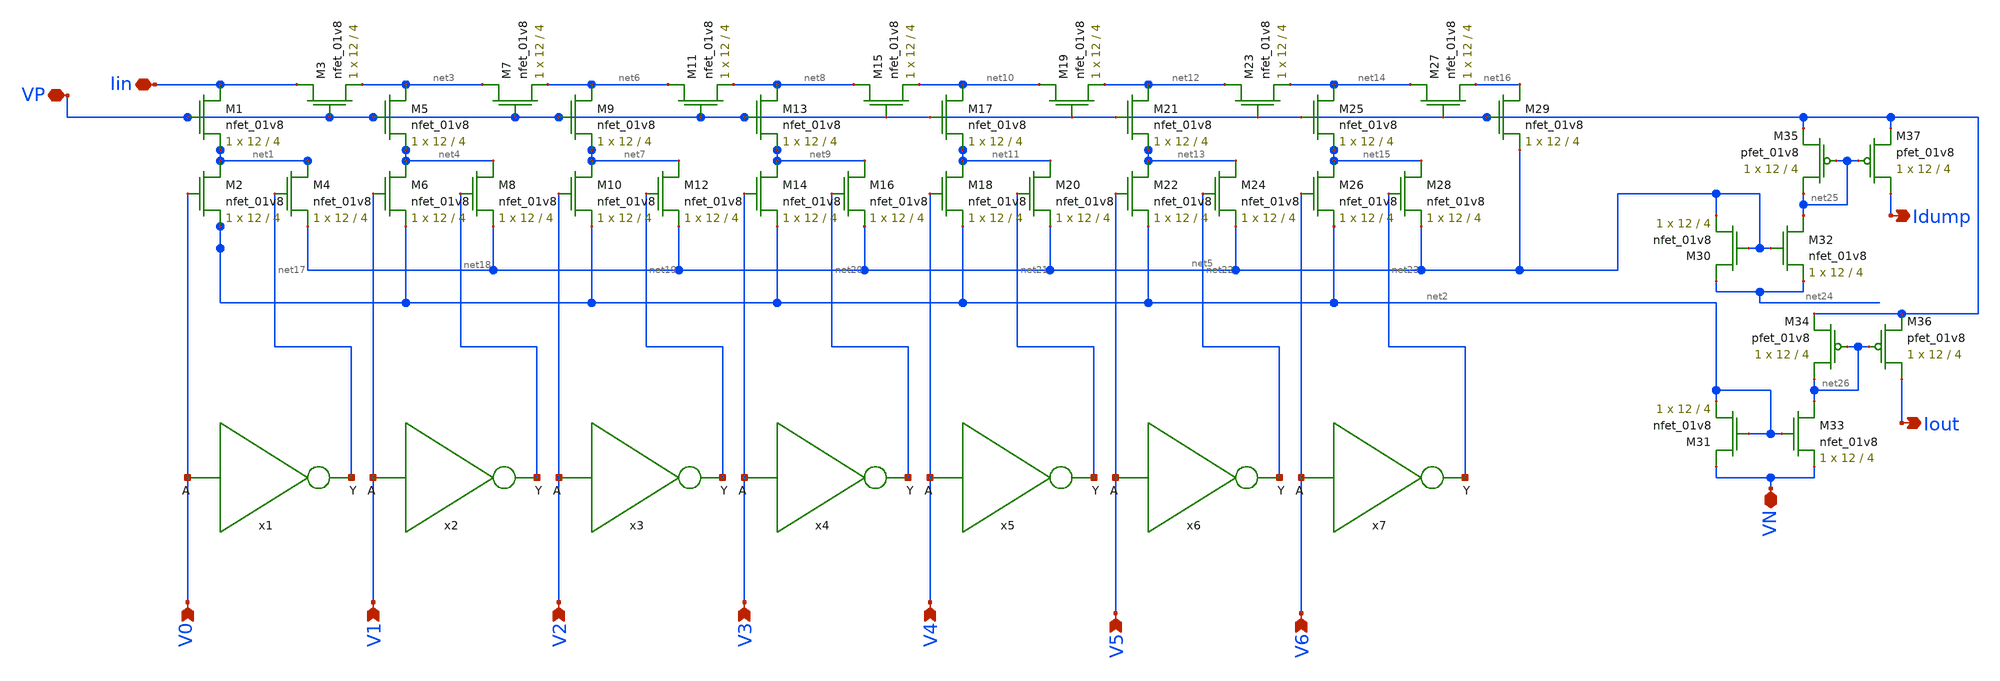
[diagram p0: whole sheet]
** sch_path: xschem/ladder.sch
**.subckt ladder V0 V1 V2 V3 V4 V5 V6 VP Iin VN Iout Idump
*.ipin V0
*.ipin V1
*.ipin V2
*.ipin V3
*.ipin V4
*.ipin V5
*.ipin V6
*.iopin VP
*.iopin Iin
*.iopin VN
*.opin Iout
*.opin Idump
XM1 Iin VP net1 GND sky130_fd_pr__nfet_01v8 L=4 W=12 nf=1 ad='int((nf+1)/2) * W/nf * 0.29' as='int((nf+2)/2) * W/nf * 0.29'
+ pd='2*int((nf+1)/2) * (W/nf + 0.29)' ps='2*int((nf+2)/2) * (W/nf + 0.29)' nrd='0.29 / W' nrs='0.29 / W'
+ sa=0 sb=0 sd=0 mult=1 m=1
XM3 Iin VP net3 GND sky130_fd_pr__nfet_01v8 L=4 W=12 nf=1 ad='int((nf+1)/2) * W/nf * 0.29' as='int((nf+2)/2) * W/nf * 0.29'
+ pd='2*int((nf+1)/2) * (W/nf + 0.29)' ps='2*int((nf+2)/2) * (W/nf + 0.29)' nrd='0.29 / W' nrs='0.29 / W'
+ sa=0 sb=0 sd=0 mult=1 m=1
XM5 net3 VP net4 GND sky130_fd_pr__nfet_01v8 L=4 W=12 nf=1 ad='int((nf+1)/2) * W/nf * 0.29' as='int((nf+2)/2) * W/nf * 0.29'
+ pd='2*int((nf+1)/2) * (W/nf + 0.29)' ps='2*int((nf+2)/2) * (W/nf + 0.29)' nrd='0.29 / W' nrs='0.29 / W'
+ sa=0 sb=0 sd=0 mult=1 m=1
XM7 net3 VP net6 GND sky130_fd_pr__nfet_01v8 L=4 W=12 nf=1 ad='int((nf+1)/2) * W/nf * 0.29' as='int((nf+2)/2) * W/nf * 0.29'
+ pd='2*int((nf+1)/2) * (W/nf + 0.29)' ps='2*int((nf+2)/2) * (W/nf + 0.29)' nrd='0.29 / W' nrs='0.29 / W'
+ sa=0 sb=0 sd=0 mult=1 m=1
XM6 net4 V1 net2 GND sky130_fd_pr__nfet_01v8 L=4 W=12 nf=1 ad='int((nf+1)/2) * W/nf * 0.29' as='int((nf+2)/2) * W/nf * 0.29'
+ pd='2*int((nf+1)/2) * (W/nf + 0.29)' ps='2*int((nf+2)/2) * (W/nf + 0.29)' nrd='0.29 / W' nrs='0.29 / W'
+ sa=0 sb=0 sd=0 mult=1 m=1
XM8 net4 net18 net5 GND sky130_fd_pr__nfet_01v8 L=4 W=12 nf=1 ad='int((nf+1)/2) * W/nf * 0.29' as='int((nf+2)/2) * W/nf * 0.29'
+ pd='2*int((nf+1)/2) * (W/nf + 0.29)' ps='2*int((nf+2)/2) * (W/nf + 0.29)' nrd='0.29 / W' nrs='0.29 / W'
+ sa=0 sb=0 sd=0 mult=1 m=1
XM2 net1 V0 net2 GND sky130_fd_pr__nfet_01v8 L=4 W=12 nf=1 ad='int((nf+1)/2) * W/nf * 0.29' as='int((nf+2)/2) * W/nf * 0.29'
+ pd='2*int((nf+1)/2) * (W/nf + 0.29)' ps='2*int((nf+2)/2) * (W/nf + 0.29)' nrd='0.29 / W' nrs='0.29 / W'
+ sa=0 sb=0 sd=0 mult=1 m=1
XM4 net1 net17 net5 GND sky130_fd_pr__nfet_01v8 L=4 W=12 nf=1 ad='int((nf+1)/2) * W/nf * 0.29' as='int((nf+2)/2) * W/nf * 0.29'
+ pd='2*int((nf+1)/2) * (W/nf + 0.29)' ps='2*int((nf+2)/2) * (W/nf + 0.29)' nrd='0.29 / W' nrs='0.29 / W'
+ sa=0 sb=0 sd=0 mult=1 m=1
XM9 net6 VP net7 GND sky130_fd_pr__nfet_01v8 L=4 W=12 nf=1 ad='int((nf+1)/2) * W/nf * 0.29' as='int((nf+2)/2) * W/nf * 0.29'
+ pd='2*int((nf+1)/2) * (W/nf + 0.29)' ps='2*int((nf+2)/2) * (W/nf + 0.29)' nrd='0.29 / W' nrs='0.29 / W'
+ sa=0 sb=0 sd=0 mult=1 m=1
XM11 net6 VP net8 GND sky130_fd_pr__nfet_01v8 L=4 W=12 nf=1 ad='int((nf+1)/2) * W/nf * 0.29' as='int((nf+2)/2) * W/nf * 0.29'
+ pd='2*int((nf+1)/2) * (W/nf + 0.29)' ps='2*int((nf+2)/2) * (W/nf + 0.29)' nrd='0.29 / W' nrs='0.29 / W'
+ sa=0 sb=0 sd=0 mult=1 m=1
XM10 net7 V2 net2 GND sky130_fd_pr__nfet_01v8 L=4 W=12 nf=1 ad='int((nf+1)/2) * W/nf * 0.29' as='int((nf+2)/2) * W/nf * 0.29'
+ pd='2*int((nf+1)/2) * (W/nf + 0.29)' ps='2*int((nf+2)/2) * (W/nf + 0.29)' nrd='0.29 / W' nrs='0.29 / W'
+ sa=0 sb=0 sd=0 mult=1 m=1
XM12 net7 net19 net5 GND sky130_fd_pr__nfet_01v8 L=4 W=12 nf=1 ad='int((nf+1)/2) * W/nf * 0.29' as='int((nf+2)/2) * W/nf * 0.29'
+ pd='2*int((nf+1)/2) * (W/nf + 0.29)' ps='2*int((nf+2)/2) * (W/nf + 0.29)' nrd='0.29 / W' nrs='0.29 / W'
+ sa=0 sb=0 sd=0 mult=1 m=1
XM13 net8 VP net9 GND sky130_fd_pr__nfet_01v8 L=4 W=12 nf=1 ad='int((nf+1)/2) * W/nf * 0.29' as='int((nf+2)/2) * W/nf * 0.29'
+ pd='2*int((nf+1)/2) * (W/nf + 0.29)' ps='2*int((nf+2)/2) * (W/nf + 0.29)' nrd='0.29 / W' nrs='0.29 / W'
+ sa=0 sb=0 sd=0 mult=1 m=1
XM15 net8 VP net10 GND sky130_fd_pr__nfet_01v8 L=4 W=12 nf=1 ad='int((nf+1)/2) * W/nf * 0.29' as='int((nf+2)/2) * W/nf * 0.29'
+ pd='2*int((nf+1)/2) * (W/nf + 0.29)' ps='2*int((nf+2)/2) * (W/nf + 0.29)' nrd='0.29 / W' nrs='0.29 / W'
+ sa=0 sb=0 sd=0 mult=1 m=1
XM14 net9 V3 net2 GND sky130_fd_pr__nfet_01v8 L=4 W=12 nf=1 ad='int((nf+1)/2) * W/nf * 0.29' as='int((nf+2)/2) * W/nf * 0.29'
+ pd='2*int((nf+1)/2) * (W/nf + 0.29)' ps='2*int((nf+2)/2) * (W/nf + 0.29)' nrd='0.29 / W' nrs='0.29 / W'
+ sa=0 sb=0 sd=0 mult=1 m=1
XM16 net9 net20 net5 GND sky130_fd_pr__nfet_01v8 L=4 W=12 nf=1 ad='int((nf+1)/2) * W/nf * 0.29' as='int((nf+2)/2) * W/nf * 0.29'
+ pd='2*int((nf+1)/2) * (W/nf + 0.29)' ps='2*int((nf+2)/2) * (W/nf + 0.29)' nrd='0.29 / W' nrs='0.29 / W'
+ sa=0 sb=0 sd=0 mult=1 m=1
XM17 net10 VP net11 GND sky130_fd_pr__nfet_01v8 L=4 W=12 nf=1 ad='int((nf+1)/2) * W/nf * 0.29' as='int((nf+2)/2) * W/nf * 0.29'
+ pd='2*int((nf+1)/2) * (W/nf + 0.29)' ps='2*int((nf+2)/2) * (W/nf + 0.29)' nrd='0.29 / W' nrs='0.29 / W'
+ sa=0 sb=0 sd=0 mult=1 m=1
XM19 net10 VP net12 GND sky130_fd_pr__nfet_01v8 L=4 W=12 nf=1 ad='int((nf+1)/2) * W/nf * 0.29' as='int((nf+2)/2) * W/nf * 0.29'
+ pd='2*int((nf+1)/2) * (W/nf + 0.29)' ps='2*int((nf+2)/2) * (W/nf + 0.29)' nrd='0.29 / W' nrs='0.29 / W'
+ sa=0 sb=0 sd=0 mult=1 m=1
XM18 net11 V4 net2 GND sky130_fd_pr__nfet_01v8 L=4 W=12 nf=1 ad='int((nf+1)/2) * W/nf * 0.29' as='int((nf+2)/2) * W/nf * 0.29'
+ pd='2*int((nf+1)/2) * (W/nf + 0.29)' ps='2*int((nf+2)/2) * (W/nf + 0.29)' nrd='0.29 / W' nrs='0.29 / W'
+ sa=0 sb=0 sd=0 mult=1 m=1
XM20 net11 net21 net5 GND sky130_fd_pr__nfet_01v8 L=4 W=12 nf=1 ad='int((nf+1)/2) * W/nf * 0.29' as='int((nf+2)/2) * W/nf * 0.29'
+ pd='2*int((nf+1)/2) * (W/nf + 0.29)' ps='2*int((nf+2)/2) * (W/nf + 0.29)' nrd='0.29 / W' nrs='0.29 / W'
+ sa=0 sb=0 sd=0 mult=1 m=1
XM21 net12 VP net13 GND sky130_fd_pr__nfet_01v8 L=4 W=12 nf=1 ad='int((nf+1)/2) * W/nf * 0.29' as='int((nf+2)/2) * W/nf * 0.29'
+ pd='2*int((nf+1)/2) * (W/nf + 0.29)' ps='2*int((nf+2)/2) * (W/nf + 0.29)' nrd='0.29 / W' nrs='0.29 / W'
+ sa=0 sb=0 sd=0 mult=1 m=1
XM23 net12 VP net14 GND sky130_fd_pr__nfet_01v8 L=4 W=12 nf=1 ad='int((nf+1)/2) * W/nf * 0.29' as='int((nf+2)/2) * W/nf * 0.29'
+ pd='2*int((nf+1)/2) * (W/nf + 0.29)' ps='2*int((nf+2)/2) * (W/nf + 0.29)' nrd='0.29 / W' nrs='0.29 / W'
+ sa=0 sb=0 sd=0 mult=1 m=1
XM22 net13 V5 net2 GND sky130_fd_pr__nfet_01v8 L=4 W=12 nf=1 ad='int((nf+1)/2) * W/nf * 0.29' as='int((nf+2)/2) * W/nf * 0.29'
+ pd='2*int((nf+1)/2) * (W/nf + 0.29)' ps='2*int((nf+2)/2) * (W/nf + 0.29)' nrd='0.29 / W' nrs='0.29 / W'
+ sa=0 sb=0 sd=0 mult=1 m=1
XM24 net13 net22 net5 GND sky130_fd_pr__nfet_01v8 L=4 W=12 nf=1 ad='int((nf+1)/2) * W/nf * 0.29' as='int((nf+2)/2) * W/nf * 0.29'
+ pd='2*int((nf+1)/2) * (W/nf + 0.29)' ps='2*int((nf+2)/2) * (W/nf + 0.29)' nrd='0.29 / W' nrs='0.29 / W'
+ sa=0 sb=0 sd=0 mult=1 m=1
XM25 net14 VP net15 GND sky130_fd_pr__nfet_01v8 L=4 W=12 nf=1 ad='int((nf+1)/2) * W/nf * 0.29' as='int((nf+2)/2) * W/nf * 0.29'
+ pd='2*int((nf+1)/2) * (W/nf + 0.29)' ps='2*int((nf+2)/2) * (W/nf + 0.29)' nrd='0.29 / W' nrs='0.29 / W'
+ sa=0 sb=0 sd=0 mult=1 m=1
XM27 net14 VP net16 GND sky130_fd_pr__nfet_01v8 L=4 W=12 nf=1 ad='int((nf+1)/2) * W/nf * 0.29' as='int((nf+2)/2) * W/nf * 0.29'
+ pd='2*int((nf+1)/2) * (W/nf + 0.29)' ps='2*int((nf+2)/2) * (W/nf + 0.29)' nrd='0.29 / W' nrs='0.29 / W'
+ sa=0 sb=0 sd=0 mult=1 m=1
XM26 net15 V6 net2 GND sky130_fd_pr__nfet_01v8 L=4 W=12 nf=1 ad='int((nf+1)/2) * W/nf * 0.29' as='int((nf+2)/2) * W/nf * 0.29'
+ pd='2*int((nf+1)/2) * (W/nf + 0.29)' ps='2*int((nf+2)/2) * (W/nf + 0.29)' nrd='0.29 / W' nrs='0.29 / W'
+ sa=0 sb=0 sd=0 mult=1 m=1
XM28 net15 net23 net5 GND sky130_fd_pr__nfet_01v8 L=4 W=12 nf=1 ad='int((nf+1)/2) * W/nf * 0.29' as='int((nf+2)/2) * W/nf * 0.29'
+ pd='2*int((nf+1)/2) * (W/nf + 0.29)' ps='2*int((nf+2)/2) * (W/nf + 0.29)' nrd='0.29 / W' nrs='0.29 / W'
+ sa=0 sb=0 sd=0 mult=1 m=1
XM29 net16 VP net5 GND sky130_fd_pr__nfet_01v8 L=4 W=12 nf=1 ad='int((nf+1)/2) * W/nf * 0.29' as='int((nf+2)/2) * W/nf * 0.29'
+ pd='2*int((nf+1)/2) * (W/nf + 0.29)' ps='2*int((nf+2)/2) * (W/nf + 0.29)' nrd='0.29 / W' nrs='0.29 / W'
+ sa=0 sb=0 sd=0 mult=1 m=1
x1 net17 V0 inverter
x2 net18 V1 inverter
x3 net19 V2 inverter
x4 net20 V3 inverter
x5 net21 V4 inverter
x6 net22 V5 inverter
x7 net23 V6 inverter
XM30 net24 net5 net5 GND sky130_fd_pr__nfet_01v8 L=4 W=12 nf=1 ad='int((nf+1)/2) * W/nf * 0.29' as='int((nf+2)/2) * W/nf * 0.29'
+ pd='2*int((nf+1)/2) * (W/nf + 0.29)' ps='2*int((nf+2)/2) * (W/nf + 0.29)' nrd='0.29 / W' nrs='0.29 / W'
+ sa=0 sb=0 sd=0 mult=1 m=1
XM31 VN net2 net2 GND sky130_fd_pr__nfet_01v8 L=4 W=12 nf=1 ad='int((nf+1)/2) * W/nf * 0.29' as='int((nf+2)/2) * W/nf * 0.29'
+ pd='2*int((nf+1)/2) * (W/nf + 0.29)' ps='2*int((nf+2)/2) * (W/nf + 0.29)' nrd='0.29 / W' nrs='0.29 / W'
+ sa=0 sb=0 sd=0 mult=1 m=1
XM32 net25 net5 net24 GND sky130_fd_pr__nfet_01v8 L=4 W=12 nf=1 ad='int((nf+1)/2) * W/nf * 0.29' as='int((nf+2)/2) * W/nf * 0.29'
+ pd='2*int((nf+1)/2) * (W/nf + 0.29)' ps='2*int((nf+2)/2) * (W/nf + 0.29)' nrd='0.29 / W' nrs='0.29 / W'
+ sa=0 sb=0 sd=0 mult=1 m=1
XM33 net26 net2 VN GND sky130_fd_pr__nfet_01v8 L=4 W=12 nf=1 ad='int((nf+1)/2) * W/nf * 0.29' as='int((nf+2)/2) * W/nf * 0.29'
+ pd='2*int((nf+1)/2) * (W/nf + 0.29)' ps='2*int((nf+2)/2) * (W/nf + 0.29)' nrd='0.29 / W' nrs='0.29 / W'
+ sa=0 sb=0 sd=0 mult=1 m=1
XM35 net25 net25 VP VDD sky130_fd_pr__pfet_01v8 L=4 W=12 nf=1 ad='int((nf+1)/2) * W/nf * 0.29' as='int((nf+2)/2) * W/nf * 0.29'
+ pd='2*int((nf+1)/2) * (W/nf + 0.29)' ps='2*int((nf+2)/2) * (W/nf + 0.29)' nrd='0.29 / W' nrs='0.29 / W'
+ sa=0 sb=0 sd=0 mult=1 m=1
XM37 Idump net25 VP VDD sky130_fd_pr__pfet_01v8 L=4 W=12 nf=1 ad='int((nf+1)/2) * W/nf * 0.29' as='int((nf+2)/2) * W/nf * 0.29'
+ pd='2*int((nf+1)/2) * (W/nf + 0.29)' ps='2*int((nf+2)/2) * (W/nf + 0.29)' nrd='0.29 / W' nrs='0.29 / W'
+ sa=0 sb=0 sd=0 mult=1 m=1
XM34 net26 net26 VP VDD sky130_fd_pr__pfet_01v8 L=4 W=12 nf=1 ad='int((nf+1)/2) * W/nf * 0.29' as='int((nf+2)/2) * W/nf * 0.29'
+ pd='2*int((nf+1)/2) * (W/nf + 0.29)' ps='2*int((nf+2)/2) * (W/nf + 0.29)' nrd='0.29 / W' nrs='0.29 / W'
+ sa=0 sb=0 sd=0 mult=1 m=1
XM36 Iout net26 VP VDD sky130_fd_pr__pfet_01v8 L=4 W=12 nf=1 ad='int((nf+1)/2) * W/nf * 0.29' as='int((nf+2)/2) * W/nf * 0.29'
+ pd='2*int((nf+1)/2) * (W/nf + 0.29)' ps='2*int((nf+2)/2) * (W/nf + 0.29)' nrd='0.29 / W' nrs='0.29 / W'
+ sa=0 sb=0 sd=0 mult=1 m=1
**.ends

* expanding   symbol:  ./inverter.sym # of pins=2
** sym_path: xschem/inverter.sym
** sch_path: xschem/inverter.sch
.subckt inverter Y A
*.ipin A
*.opin Y
XM1 Y A VDD VDD sky130_fd_pr__pfet_01v8 L=0.15 W=1 nf=1 ad='int((nf+1)/2) * W/nf * 0.29' as='int((nf+2)/2) * W/nf * 0.29'
+ pd='2*int((nf+1)/2) * (W/nf + 0.29)' ps='2*int((nf+2)/2) * (W/nf + 0.29)' nrd='0.29 / W' nrs='0.29 / W'
+ sa=0 sb=0 sd=0 mult=1 m=1
XM2 Y A GND GND sky130_fd_pr__nfet_01v8 L=0.15 W=1 nf=1 ad='int((nf+1)/2) * W/nf * 0.29' as='int((nf+2)/2) * W/nf * 0.29'
+ pd='2*int((nf+1)/2) * (W/nf + 0.29)' ps='2*int((nf+2)/2) * (W/nf + 0.29)' nrd='0.29 / W' nrs='0.29 / W'
+ sa=0 sb=0 sd=0 mult=1 m=1
.ends

.GLOBAL GND
.GLOBAL VDD
.end
